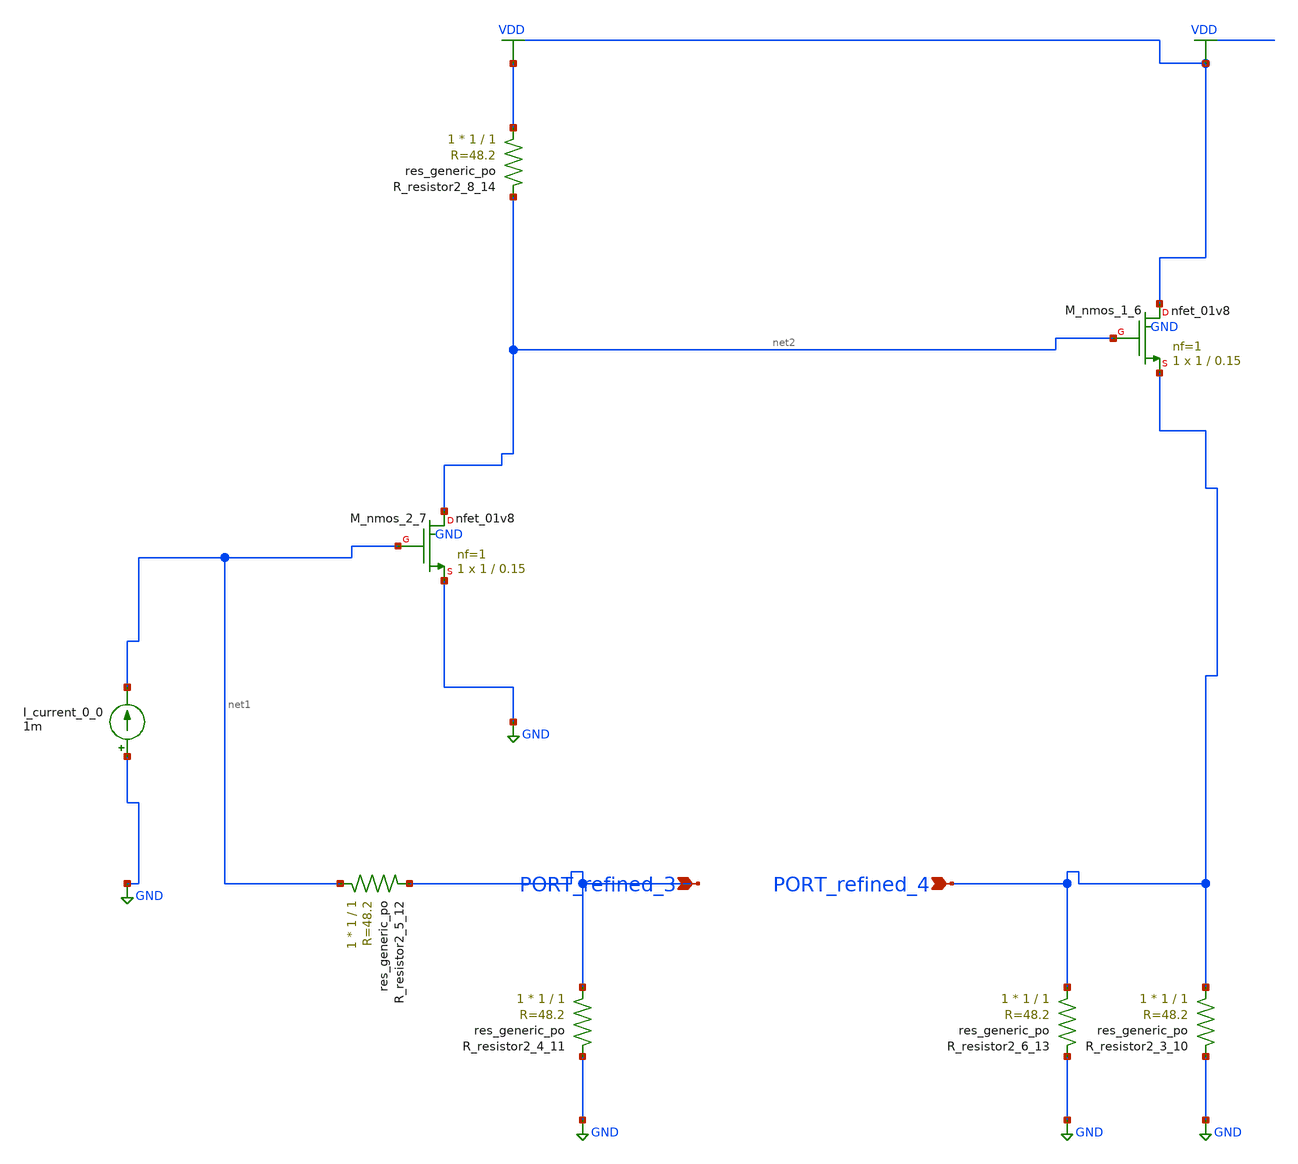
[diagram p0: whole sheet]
** sch_path: schematics/AMSNet/584.sch
**.subckt 584 PORT_refined_3 PORT_refined_4
*.ipin PORT_refined_3
*.ipin PORT_refined_4
I_current_0_0 GND net1 1m
XM_nmos_1_6 VDD net2 PORT_refined_4 GND sky130_fd_pr__nfet_01v8 L=0.15 W=1 nf=1 ad='int((1 + 1)/2) * 1 / 1 * 0.29'
+ as='int((1 + 2)/2) * 1 / 1 * 0.29' pd='2*int((1 + 1)/2) * (1 / 1 + 0.29)' ps='2*int((1 + 2)/2) * (1 / 1 + 0.29)'
+ nrd='0.29 / 1 ' nrs='0.29 / 1 ' sa=0 sb=0 sd=0 mult=1 m=1
XM_nmos_2_7 net2 net1 GND GND sky130_fd_pr__nfet_01v8 L=0.15 W=1 nf=1 ad='int((1 + 1)/2) * 1 / 1 * 0.29'
+ as='int((1 + 2)/2) * 1 / 1 * 0.29' pd='2*int((1 + 1)/2) * (1 / 1 + 0.29)' ps='2*int((1 + 2)/2) * (1 / 1 + 0.29)'
+ nrd='0.29 / 1 ' nrs='0.29 / 1 ' sa=0 sb=0 sd=0 mult=1 m=1
XR_resistor2_3_10 PORT_refined_4 GND sky130_fd_pr__res_generic_po W=1 L=1 m=1
XR_resistor2_4_11 PORT_refined_3 GND sky130_fd_pr__res_generic_po W=1 L=1 m=1
XR_resistor2_5_12 net1 PORT_refined_3 sky130_fd_pr__res_generic_po W=1 L=1 m=1
XR_resistor2_6_13 PORT_refined_4 GND sky130_fd_pr__res_generic_po W=1 L=1 m=1
XR_resistor2_8_14 VDD net2 sky130_fd_pr__res_generic_po W=1 L=1 m=1
**.ends
.GLOBAL GND
.GLOBAL VDD
.end
